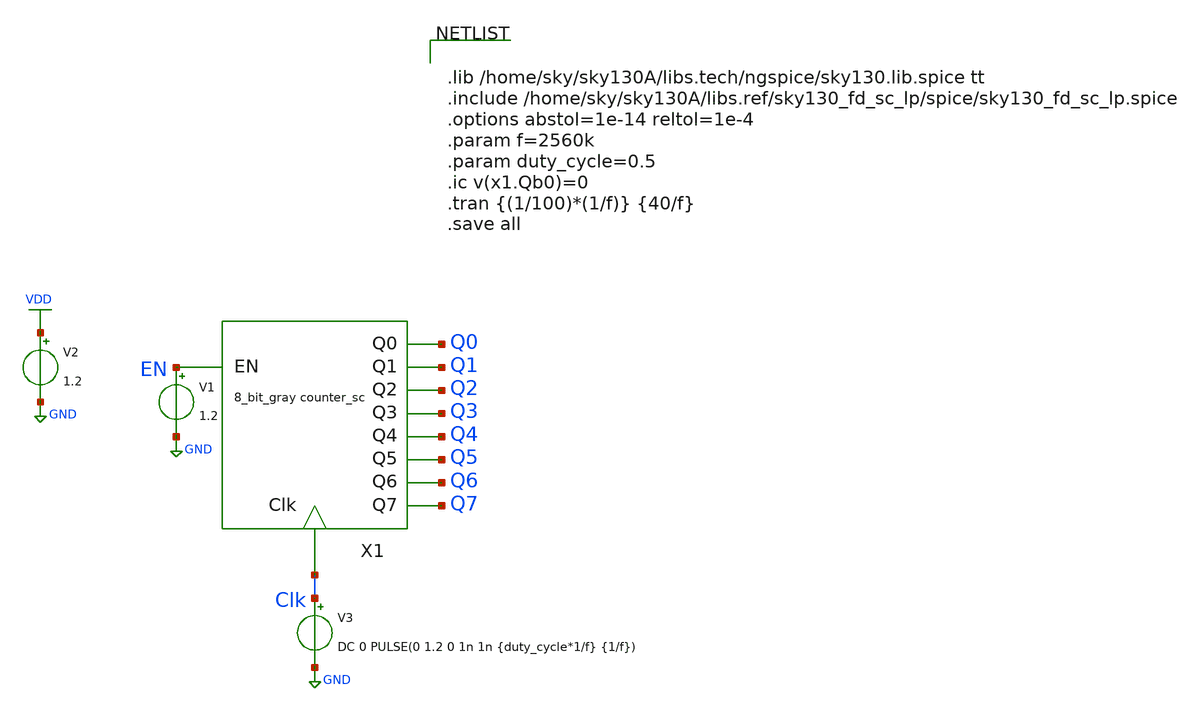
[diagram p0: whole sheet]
** sch_path: xschem/8_bit_gray_counter/8_bit_gray_counter_sc_Ip_tc.sch
**.subckt 8_bit_gray_counter_sc_Ip_tc
V3 Clk GND DC 0 PULSE(0 1.2 0 1n 1n {duty_cycle*1/f} {1/f})
V1 EN GND 1.2
V2 VDD GND 1.2
X1 EN Q1 Q6 Clk Q0 Q2 Q3 Q4 Q5 Q7 8_bit_gray_counter_sc_Ip
**** begin user architecture code


.lib /home/sky/sky130A/libs.tech/ngspice/sky130.lib.spice tt
.include /home/sky/sky130A/libs.ref/sky130_fd_sc_lp/spice/sky130_fd_sc_lp.spice
.options abstol=1e-14 reltol=1e-4
.param f=2560k
.param duty_cycle=0.5
.ic v(x1.Qb0)=0
.tran {(1/100)*(1/f)} {40/f}
.save all


**** end user architecture code
**.ends
.GLOBAL GND
.GLOBAL VDD
.end
